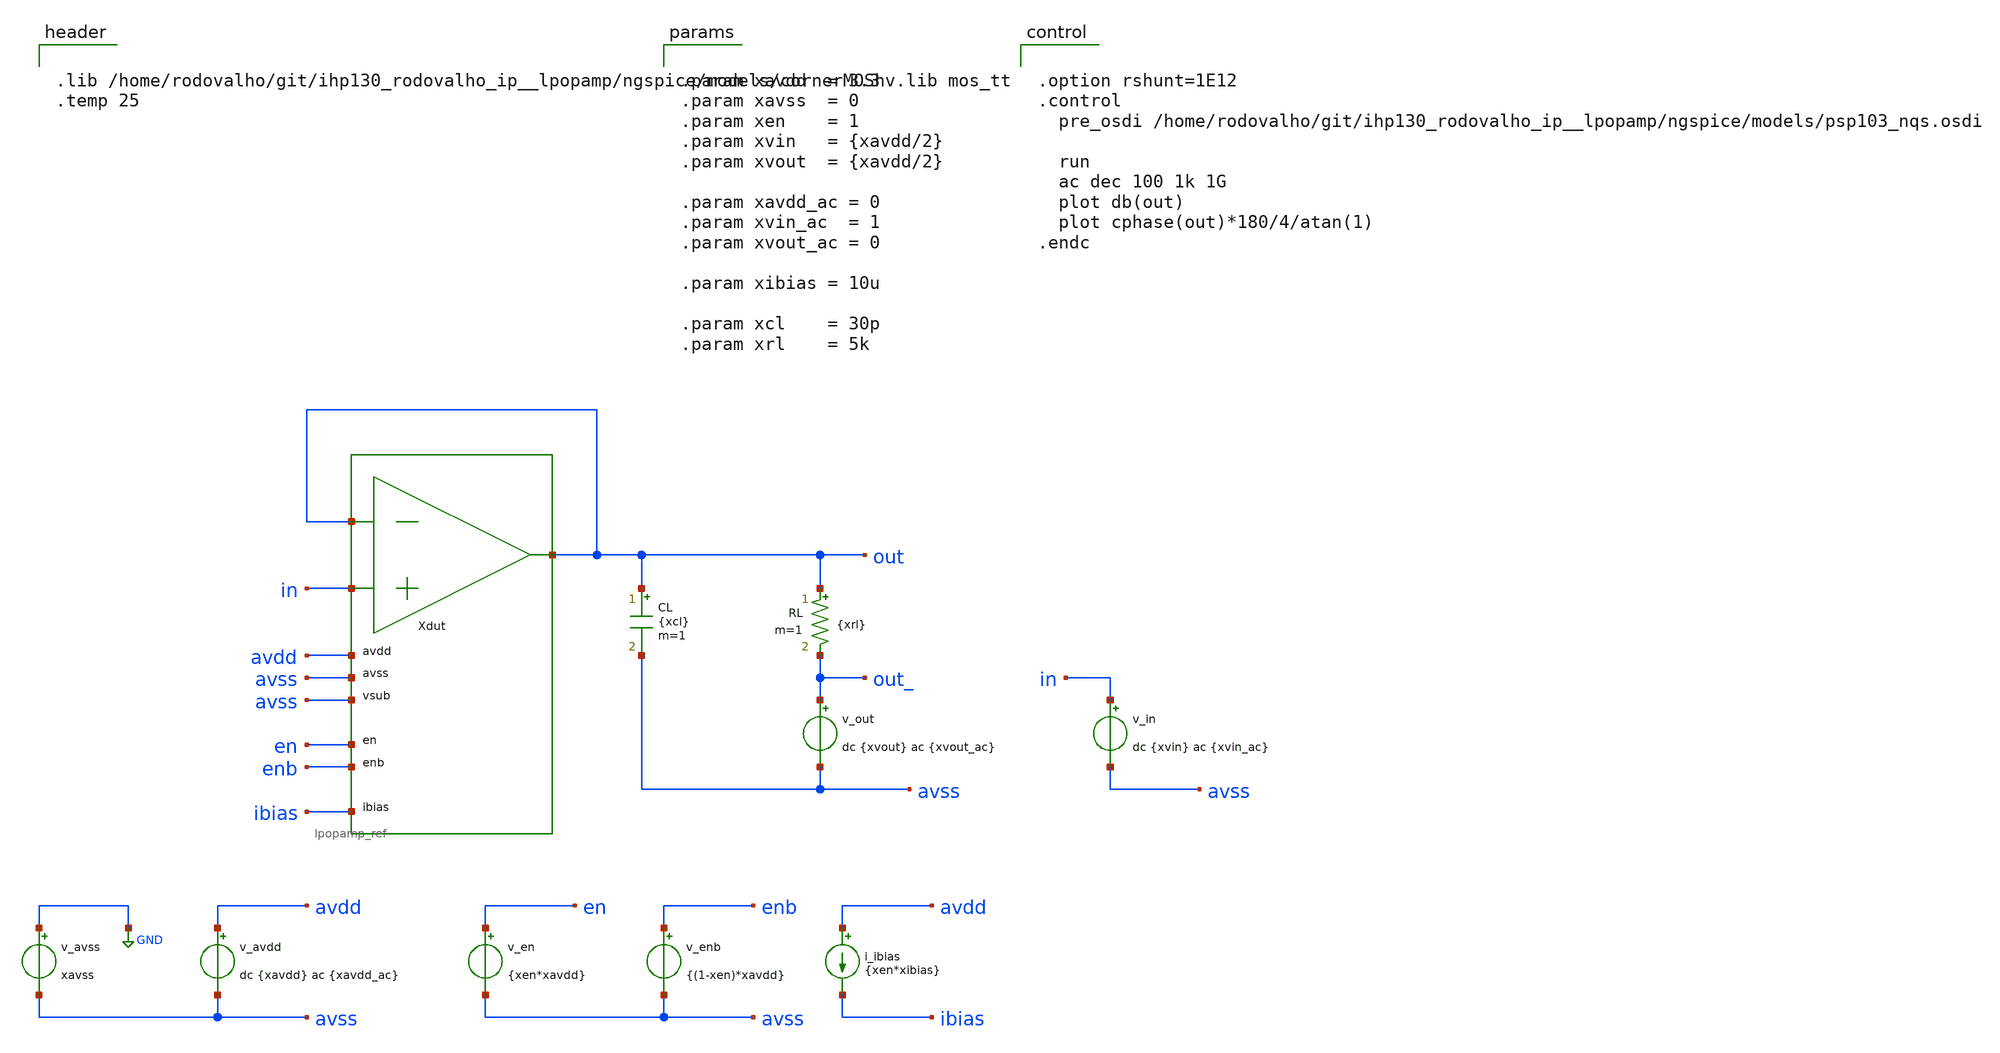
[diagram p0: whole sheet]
** sch_path: xschem/tb_lpopamp_buf_ac.sch
**.subckt tb_lpopamp_buf_ac
Xdut out in out avdd avss avss en enb ibias lpopamp_ref
v_avss GND avss xavss
v_avdd avdd avss dc {xavdd} ac {xavdd_ac}
v_in in avss dc {xvin} ac {xvin_ac}
v_en en avss {xen*xavdd}
v_enb enb avss {(1-xen)*xavdd}
i_ibias avdd ibias {xen*xibias}
CL out avss {xcl} m=1
v_out out_ avss dc {xvout} ac {xvout_ac}
RL out out_ {xrl} m=1
**** begin user architecture code


.lib /home/rodovalho/git/ihp130_rodovalho_ip__lpopamp/ngspice/models/cornerMOShv.lib mos_tt
.temp 25




.option rshunt=1E12
.control
  pre_osdi /home/rodovalho/git/ihp130_rodovalho_ip__lpopamp/ngspice/models/psp103_nqs.osdi

  run
  ac dec 100 1k 1G
  plot db(out)
  plot cphase(out)*180/4/atan(1)
.endc




.param xavdd  = 3.3
.param xavss  = 0
.param xen    = 1
.param xvin   = {xavdd/2}
.param xvout  = {xavdd/2}

.param xavdd_ac = 0
.param xvin_ac  = 1
.param xvout_ac = 0

.param xibias = 10u

.param xcl    = 30p
.param xrl    = 5k


**** end user architecture code
**.ends
.GLOBAL GND
.end
